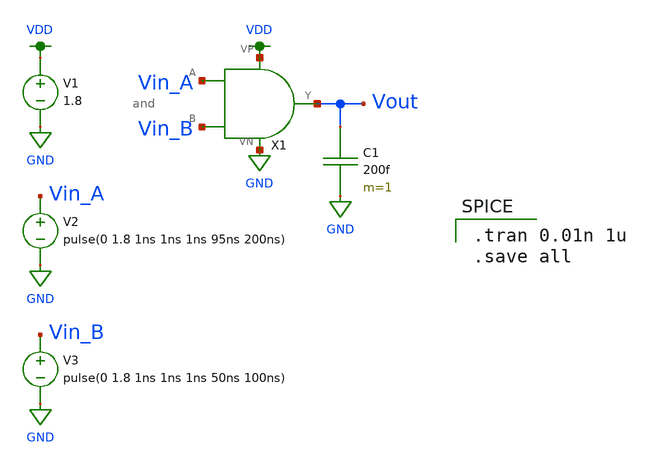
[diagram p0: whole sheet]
** sch_path: and_gate/schematics/and_tran.sch
**.subckt and_tran
V1 VDD GND 1.8
V2 Vin_A GND pulse(0 1.8 1ns 1ns 1ns 95ns 200ns)
V3 Vin_B GND pulse(0 1.8 1ns 1ns 1ns 50ns 100ns)
C1 Vout GND 200f m=1
X1 Vout GND VDD Vin_A Vin_B and
**** begin user architecture code

.option wnflag=1
.lib ~/skywater/skywater-pdk/libraries/sky130_fd_pr_ngspice/latest/models/sky130.lib.spice tt


.tran 0.01n 1u
.save all

**** end user architecture code
**.ends
.GLOBAL VDD
.GLOBAL GND
.end
